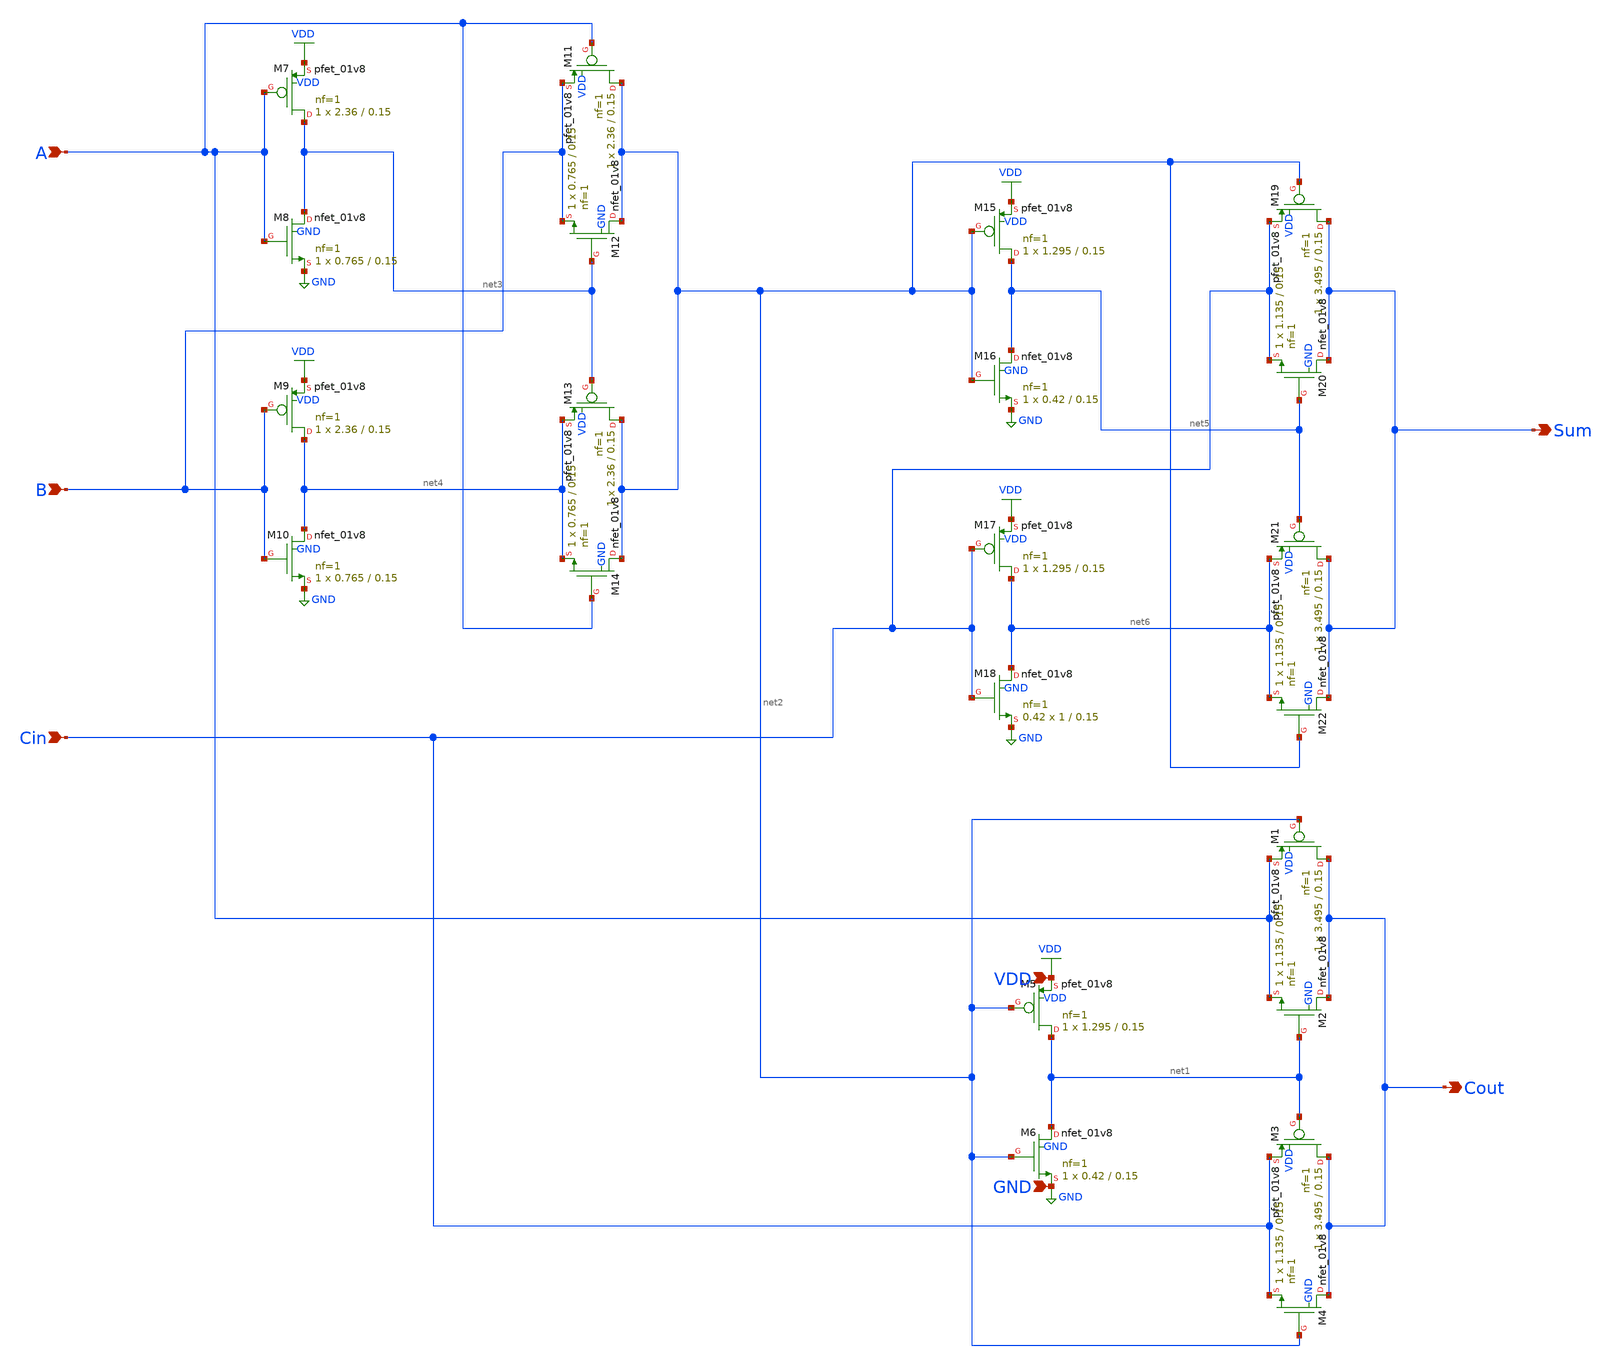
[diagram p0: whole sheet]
** sch_path: transmission_gate/schematic/fulladder.sch
**.subckt fulladder Cout A B Cin Sum VDD GND
*.opin Cout
*.ipin A
*.ipin B
*.ipin Cin
*.opin Sum
*.ipin VDD
*.ipin GND
XM1 Cout net2 A VDD sky130_fd_pr__pfet_01v8 L=0.15 W=3.495 nf=1 ad='int((1 + 1)/2) * 3.495 / 1 * 0.29'
+ as='int((1 + 2)/2) * 3.495 / 1 * 0.29' pd='2*int((1 + 1)/2) * (3.495 / 1 + 0.29)' ps='2*int((1 + 2)/2) * (3.495 / 1 + 0.29)'
+ nrd='0.29 / 3.495 ' nrs='0.29 / 3.495 ' sa=0 sb=0 sd=0 mult=1 m=1
XM2 Cout net1 A GND sky130_fd_pr__nfet_01v8 L=0.15 W=1.135 nf=1 ad='int((1 + 1)/2) * 1.135 / 1 * 0.29'
+ as='int((1 + 2)/2) * 1.135 / 1 * 0.29' pd='2*int((1 + 1)/2) * (1.135 / 1 + 0.29)' ps='2*int((1 + 2)/2) * (1.135 / 1 + 0.29)'
+ nrd='0.29 / 1.135 ' nrs='0.29 / 1.135 ' sa=0 sb=0 sd=0 mult=1 m=1
XM3 Cout net1 Cin VDD sky130_fd_pr__pfet_01v8 L=0.15 W=3.495 nf=1 ad='int((1 + 1)/2) * 3.495 / 1 * 0.29'
+ as='int((1 + 2)/2) * 3.495 / 1 * 0.29' pd='2*int((1 + 1)/2) * (3.495 / 1 + 0.29)' ps='2*int((1 + 2)/2) * (3.495 / 1 + 0.29)'
+ nrd='0.29 / 3.495 ' nrs='0.29 / 3.495 ' sa=0 sb=0 sd=0 mult=1 m=1
XM4 Cout net2 Cin GND sky130_fd_pr__nfet_01v8 L=0.15 W=1.135 nf=1 ad='int((1 + 1)/2) * 1.135 / 1 * 0.29'
+ as='int((1 + 2)/2) * 1.135 / 1 * 0.29' pd='2*int((1 + 1)/2) * (1.135 / 1 + 0.29)' ps='2*int((1 + 2)/2) * (1.135 / 1 + 0.29)'
+ nrd='0.29 / 1.135 ' nrs='0.29 / 1.135 ' sa=0 sb=0 sd=0 mult=1 m=1
XM5 net1 net2 VDD VDD sky130_fd_pr__pfet_01v8 L=0.15 W=1.295 nf=1 ad='int((1 + 1)/2) * 1.295 / 1 * 0.29'
+ as='int((1 + 2)/2) * 1.295 / 1 * 0.29' pd='2*int((1 + 1)/2) * (1.295 / 1 + 0.29)' ps='2*int((1 + 2)/2) * (1.295 / 1 + 0.29)'
+ nrd='0.29 / 1.295 ' nrs='0.29 / 1.295 ' sa=0 sb=0 sd=0 mult=1 m=1
XM6 net1 net2 GND GND sky130_fd_pr__nfet_01v8 L=0.15 W=0.42 nf=1 ad='int((1 + 1)/2) * 0.42 / 1 * 0.29'
+ as='int((1 + 2)/2) * 0.42 / 1 * 0.29' pd='2*int((1 + 1)/2) * (0.42 / 1 + 0.29)' ps='2*int((1 + 2)/2) * (0.42 / 1 + 0.29)'
+ nrd='0.29 / 0.42 ' nrs='0.29 / 0.42 ' sa=0 sb=0 sd=0 mult=1 m=1
XM7 net3 A VDD VDD sky130_fd_pr__pfet_01v8 L=0.15 W=2.36 nf=1 ad='int((1 + 1)/2) * 2.36 / 1 * 0.29' as='int((1 + 2)/2) * 2.36 / 1 * 0.29'
+ pd='2*int((1 + 1)/2) * (2.36 / 1 + 0.29)' ps='2*int((1 + 2)/2) * (2.36 / 1 + 0.29)' nrd='0.29 / 2.36 '
+ nrs='0.29 / 2.36 ' sa=0 sb=0 sd=0 mult=1 m=1
XM8 net3 A GND GND sky130_fd_pr__nfet_01v8 L=0.15 W=0.765 nf=1 ad='int((1 + 1)/2) * 0.765 / 1 * 0.29'
+ as='int((1 + 2)/2) * 0.765 / 1 * 0.29' pd='2*int((1 + 1)/2) * (0.765 / 1 + 0.29)' ps='2*int((1 + 2)/2) * (0.765 / 1 + 0.29)'
+ nrd='0.29 / 0.765 ' nrs='0.29 / 0.765 ' sa=0 sb=0 sd=0 mult=1 m=1
XM9 net4 B VDD VDD sky130_fd_pr__pfet_01v8 L=0.15 W=2.36 nf=1 ad='int((1 + 1)/2) * 2.36 / 1 * 0.29' as='int((1 + 2)/2) * 2.36 / 1 * 0.29'
+ pd='2*int((1 + 1)/2) * (2.36 / 1 + 0.29)' ps='2*int((1 + 2)/2) * (2.36 / 1 + 0.29)' nrd='0.29 / 2.36 '
+ nrs='0.29 / 2.36 ' sa=0 sb=0 sd=0 mult=1 m=1
XM10 net4 B GND GND sky130_fd_pr__nfet_01v8 L=0.15 W=0.765 nf=1 ad='int((1 + 1)/2) * 0.765 / 1 * 0.29'
+ as='int((1 + 2)/2) * 0.765 / 1 * 0.29' pd='2*int((1 + 1)/2) * (0.765 / 1 + 0.29)' ps='2*int((1 + 2)/2) * (0.765 / 1 + 0.29)'
+ nrd='0.29 / 0.765 ' nrs='0.29 / 0.765 ' sa=0 sb=0 sd=0 mult=1 m=1
XM11 net2 A B VDD sky130_fd_pr__pfet_01v8 L=0.15 W=2.36 nf=1 ad='int((1 + 1)/2) * 2.36 / 1 * 0.29' as='int((1 + 2)/2) * 2.36 / 1 * 0.29'
+ pd='2*int((1 + 1)/2) * (2.36 / 1 + 0.29)' ps='2*int((1 + 2)/2) * (2.36 / 1 + 0.29)' nrd='0.29 / 2.36 '
+ nrs='0.29 / 2.36 ' sa=0 sb=0 sd=0 mult=1 m=1
XM12 net2 net3 B GND sky130_fd_pr__nfet_01v8 L=0.15 W=0.765 nf=1 ad='int((1 + 1)/2) * 0.765 / 1 * 0.29'
+ as='int((1 + 2)/2) * 0.765 / 1 * 0.29' pd='2*int((1 + 1)/2) * (0.765 / 1 + 0.29)' ps='2*int((1 + 2)/2) * (0.765 / 1 + 0.29)'
+ nrd='0.29 / 0.765 ' nrs='0.29 / 0.765 ' sa=0 sb=0 sd=0 mult=1 m=1
XM13 net2 net3 net4 VDD sky130_fd_pr__pfet_01v8 L=0.15 W=2.36 nf=1 ad='int((1 + 1)/2) * 2.36 / 1 * 0.29'
+ as='int((1 + 2)/2) * 2.36 / 1 * 0.29' pd='2*int((1 + 1)/2) * (2.36 / 1 + 0.29)' ps='2*int((1 + 2)/2) * (2.36 / 1 + 0.29)'
+ nrd='0.29 / 2.36 ' nrs='0.29 / 2.36 ' sa=0 sb=0 sd=0 mult=1 m=1
XM14 net2 A net4 GND sky130_fd_pr__nfet_01v8 L=0.15 W=0.765 nf=1 ad='int((1 + 1)/2) * 0.765 / 1 * 0.29'
+ as='int((1 + 2)/2) * 0.765 / 1 * 0.29' pd='2*int((1 + 1)/2) * (0.765 / 1 + 0.29)' ps='2*int((1 + 2)/2) * (0.765 / 1 + 0.29)'
+ nrd='0.29 / 0.765 ' nrs='0.29 / 0.765 ' sa=0 sb=0 sd=0 mult=1 m=1
XM15 net5 net2 VDD VDD sky130_fd_pr__pfet_01v8 L=0.15 W=1.295 nf=1 ad='int((1 + 1)/2) * 1.295 / 1 * 0.29'
+ as='int((1 + 2)/2) * 1.295 / 1 * 0.29' pd='2*int((1 + 1)/2) * (1.295 / 1 + 0.29)' ps='2*int((1 + 2)/2) * (1.295 / 1 + 0.29)'
+ nrd='0.29 / 1.295 ' nrs='0.29 / 1.295 ' sa=0 sb=0 sd=0 mult=1 m=1
XM16 net5 net2 GND GND sky130_fd_pr__nfet_01v8 L=0.15 W=0.42 nf=1 ad='int((1 + 1)/2) * 0.42 / 1 * 0.29'
+ as='int((1 + 2)/2) * 0.42 / 1 * 0.29' pd='2*int((1 + 1)/2) * (0.42 / 1 + 0.29)' ps='2*int((1 + 2)/2) * (0.42 / 1 + 0.29)'
+ nrd='0.29 / 0.42 ' nrs='0.29 / 0.42 ' sa=0 sb=0 sd=0 mult=1 m=1
XM17 net6 Cin VDD VDD sky130_fd_pr__pfet_01v8 L=0.15 W=1.295 nf=1 ad='int((1 + 1)/2) * 1.295 / 1 * 0.29'
+ as='int((1 + 2)/2) * 1.295 / 1 * 0.29' pd='2*int((1 + 1)/2) * (1.295 / 1 + 0.29)' ps='2*int((1 + 2)/2) * (1.295 / 1 + 0.29)'
+ nrd='0.29 / 1.295 ' nrs='0.29 / 1.295 ' sa=0 sb=0 sd=0 mult=1 m=1
XM18 net6 Cin GND GND sky130_fd_pr__nfet_01v8 L=0.15 W=1 nf=1 ad='int((1 + 1)/2) * 1 / 1 * 0.29' as='int((1 + 2)/2) * 1 / 1 * 0.29'
+ pd='2*int((1 + 1)/2) * (1 / 1 + 0.29)' ps='2*int((1 + 2)/2) * (1 / 1 + 0.29)' nrd='0.29 / 1 ' nrs='0.29 / 1 '
+ sa=0 sb=0 sd=0 mult=0.42 m=0.42
XM19 Sum net2 Cin VDD sky130_fd_pr__pfet_01v8 L=0.15 W=3.495 nf=1 ad='int((1 + 1)/2) * 3.495 / 1 * 0.29'
+ as='int((1 + 2)/2) * 3.495 / 1 * 0.29' pd='2*int((1 + 1)/2) * (3.495 / 1 + 0.29)' ps='2*int((1 + 2)/2) * (3.495 / 1 + 0.29)'
+ nrd='0.29 / 3.495 ' nrs='0.29 / 3.495 ' sa=0 sb=0 sd=0 mult=1 m=1
XM20 Sum net5 Cin GND sky130_fd_pr__nfet_01v8 L=0.15 W=1.135 nf=1 ad='int((1 + 1)/2) * 1.135 / 1 * 0.29'
+ as='int((1 + 2)/2) * 1.135 / 1 * 0.29' pd='2*int((1 + 1)/2) * (1.135 / 1 + 0.29)' ps='2*int((1 + 2)/2) * (1.135 / 1 + 0.29)'
+ nrd='0.29 / 1.135 ' nrs='0.29 / 1.135 ' sa=0 sb=0 sd=0 mult=1 m=1
XM21 Sum net5 net6 VDD sky130_fd_pr__pfet_01v8 L=0.15 W=3.495 nf=1 ad='int((1 + 1)/2) * 3.495 / 1 * 0.29'
+ as='int((1 + 2)/2) * 3.495 / 1 * 0.29' pd='2*int((1 + 1)/2) * (3.495 / 1 + 0.29)' ps='2*int((1 + 2)/2) * (3.495 / 1 + 0.29)'
+ nrd='0.29 / 3.495 ' nrs='0.29 / 3.495 ' sa=0 sb=0 sd=0 mult=1 m=1
XM22 Sum net2 net6 GND sky130_fd_pr__nfet_01v8 L=0.15 W=1.135 nf=1 ad='int((1 + 1)/2) * 1.135 / 1 * 0.29'
+ as='int((1 + 2)/2) * 1.135 / 1 * 0.29' pd='2*int((1 + 1)/2) * (1.135 / 1 + 0.29)' ps='2*int((1 + 2)/2) * (1.135 / 1 + 0.29)'
+ nrd='0.29 / 1.135 ' nrs='0.29 / 1.135 ' sa=0 sb=0 sd=0 mult=1 m=1
**.ends
.GLOBAL GND
.GLOBAL VDD
.end
